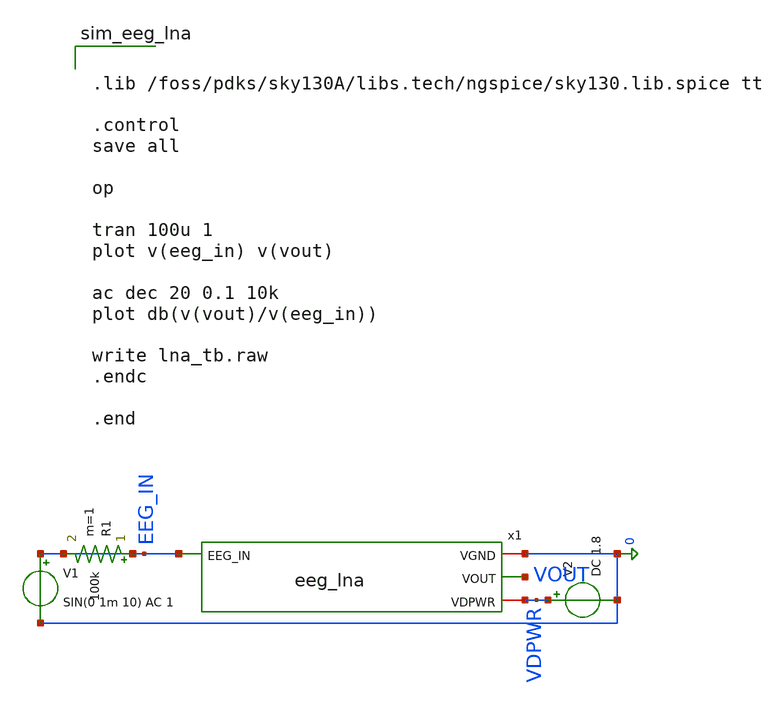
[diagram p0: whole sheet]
** sch_path: xschem/eeg_lna_tb.sch
**.subckt eeg_lna_tb
V1 EEG_IN 0 SIN(0 1m 10) AC 1
V2 VDPWR 0 DC 1.8
x1 EEG_IN 0 VOUT VDPWR eeg_lna
R1 EEG_IN EEG_IN 100k m=1
**** begin user architecture code


.lib /foss/pdks/sky130A/libs.tech/ngspice/sky130.lib.spice tt

.control
save all

op

tran 100u 1
plot v(eeg_in) v(vout)

ac dec 20 0.1 10k
plot db(v(vout)/v(eeg_in))

write lna_tb.raw
.endc

.end


**** end user architecture code
**.ends

* expanding   symbol:  eeg_lna.sym # of pins=4
** sym_path: xschem/eeg_lna.sym
** sch_path: xschem/eeg_lna.sch
.subckt eeg_lna EEG_IN VGND VOUT VDPWR
*.iopin VGND
*.ipin EEG_IN
*.iopin VDPWR
*.opin VOUT
XM1 MIRROR_BIAS_N MIRROR_BIAS_N VGND VGND sky130_fd_pr__nfet_01v8 L=1.0 W=20 nf=1 ad='int((1 + 1)/2) * 20 / 1 * 0.29'
+ as='int((1 + 2)/2) * 20 / 1 * 0.29' pd='2*int((1 + 1)/2) * (20 / 1 + 0.29)' ps='2*int((1 + 2)/2) * (20 / 1 + 0.29)'
+ nrd='0.29 / 20 ' nrs='0.29 / 20 ' sa=0 sb=0 sd=0 mult=1 m=1
XM2 VOUT MIRROR_BIAS_N VGND VGND sky130_fd_pr__nfet_01v8 L=1.0 W=20 nf=1 ad='int((1 + 1)/2) * 20 / 1 * 0.29'
+ as='int((1 + 2)/2) * 20 / 1 * 0.29' pd='2*int((1 + 1)/2) * (20 / 1 + 0.29)' ps='2*int((1 + 2)/2) * (20 / 1 + 0.29)'
+ nrd='0.29 / 20 ' nrs='0.29 / 20 ' sa=0 sb=0 sd=0 mult=1 m=1
XM3 MIRROR_BIAS_N VIN_P TAIL_P VDPWR sky130_fd_pr__pfet_01v8 L=1.0 W=40 nf=1 ad='int((1 + 1)/2) * 40 / 1 * 0.29'
+ as='int((1 + 2)/2) * 40 / 1 * 0.29' pd='2*int((1 + 1)/2) * (40 / 1 + 0.29)' ps='2*int((1 + 2)/2) * (40 / 1 + 0.29)'
+ nrd='0.29 / 40 ' nrs='0.29 / 40 ' sa=0 sb=0 sd=0 mult=1 m=1
XM4 VOUT VIN_N TAIL_P VDPWR sky130_fd_pr__pfet_01v8 L=1.0 W=40 nf=1 ad='int((1 + 1)/2) * 40 / 1 * 0.29'
+ as='int((1 + 2)/2) * 40 / 1 * 0.29' pd='2*int((1 + 1)/2) * (40 / 1 + 0.29)' ps='2*int((1 + 2)/2) * (40 / 1 + 0.29)'
+ nrd='0.29 / 40 ' nrs='0.29 / 40 ' sa=0 sb=0 sd=0 mult=1 m=1
XM5 TAIL_P BIAS_P VDPWR VDPWR sky130_fd_pr__pfet_01v8 L=1.0 W=30 nf=1 ad='int((1 + 1)/2) * 30 / 1 * 0.29'
+ as='int((1 + 2)/2) * 30 / 1 * 0.29' pd='2*int((1 + 1)/2) * (30 / 1 + 0.29)' ps='2*int((1 + 2)/2) * (30 / 1 + 0.29)'
+ nrd='0.29 / 30 ' nrs='0.29 / 30 ' sa=0 sb=0 sd=0 mult=1 m=1
XM6 BIAS_P BIAS_P VDPWR VDPWR sky130_fd_pr__pfet_01v8 L=1.0 W=10 nf=1 ad='int((1 + 1)/2) * 10 / 1 * 0.29'
+ as='int((1 + 2)/2) * 10 / 1 * 0.29' pd='2*int((1 + 1)/2) * (10 / 1 + 0.29)' ps='2*int((1 + 2)/2) * (10 / 1 + 0.29)'
+ nrd='0.29 / 10 ' nrs='0.29 / 10 ' sa=0 sb=0 sd=0 mult=1 m=1
XM7 BIAS_P BIAS_P VGND VGND sky130_fd_pr__nfet_01v8 L=1.0 W=5 nf=1 ad='int((1 + 1)/2) * 5 / 1 * 0.29'
+ as='int((1 + 2)/2) * 5 / 1 * 0.29' pd='2*int((1 + 1)/2) * (5 / 1 + 0.29)' ps='2*int((1 + 2)/2) * (5 / 1 + 0.29)'
+ nrd='0.29 / 5 ' nrs='0.29 / 5 ' sa=0 sb=0 sd=0 mult=1 m=1
XCIN VIN_P EEG_IN sky130_fd_pr__cap_mim_m3_1 W=40 L=40 MF=1 m=1
RF VOUT VIN_N 100k m=1
RG VIN_N BIAS_P 100k m=1
x1 VIN_P BIAS_P pseudo_res
.ends


* expanding   symbol:  pseudo_res.sym # of pins=2
** sym_path: xschem/pseudo_res.sym
** sch_path: xschem/pseudo_res.sch
.subckt pseudo_res B A
*.iopin A
*.iopin B
XM1 B B A A sky130_fd_pr__pfet_01v8 L=10 W=0.42 nf=1 ad='int((1 + 1)/2) * 0.42 / 1 * 0.29' as='int((1 + 2)/2) * 0.42 / 1 * 0.29'
+ pd='2*int((1 + 1)/2) * (0.42 / 1 + 0.29)' ps='2*int((1 + 2)/2) * (0.42 / 1 + 0.29)' nrd='0.29 / 0.42 '
+ nrs='0.29 / 0.42 ' sa=0 sb=0 sd=0 mult=1 m=1
XM2 A A B B sky130_fd_pr__pfet_01v8 L=10 W=0.42 nf=1 ad='int((1 + 1)/2) * 0.42 / 1 * 0.29' as='int((1 + 2)/2) * 0.42 / 1 * 0.29'
+ pd='2*int((1 + 1)/2) * (0.42 / 1 + 0.29)' ps='2*int((1 + 2)/2) * (0.42 / 1 + 0.29)' nrd='0.29 / 0.42 '
+ nrs='0.29 / 0.42 ' sa=0 sb=0 sd=0 mult=1 m=1
.ends

.end
